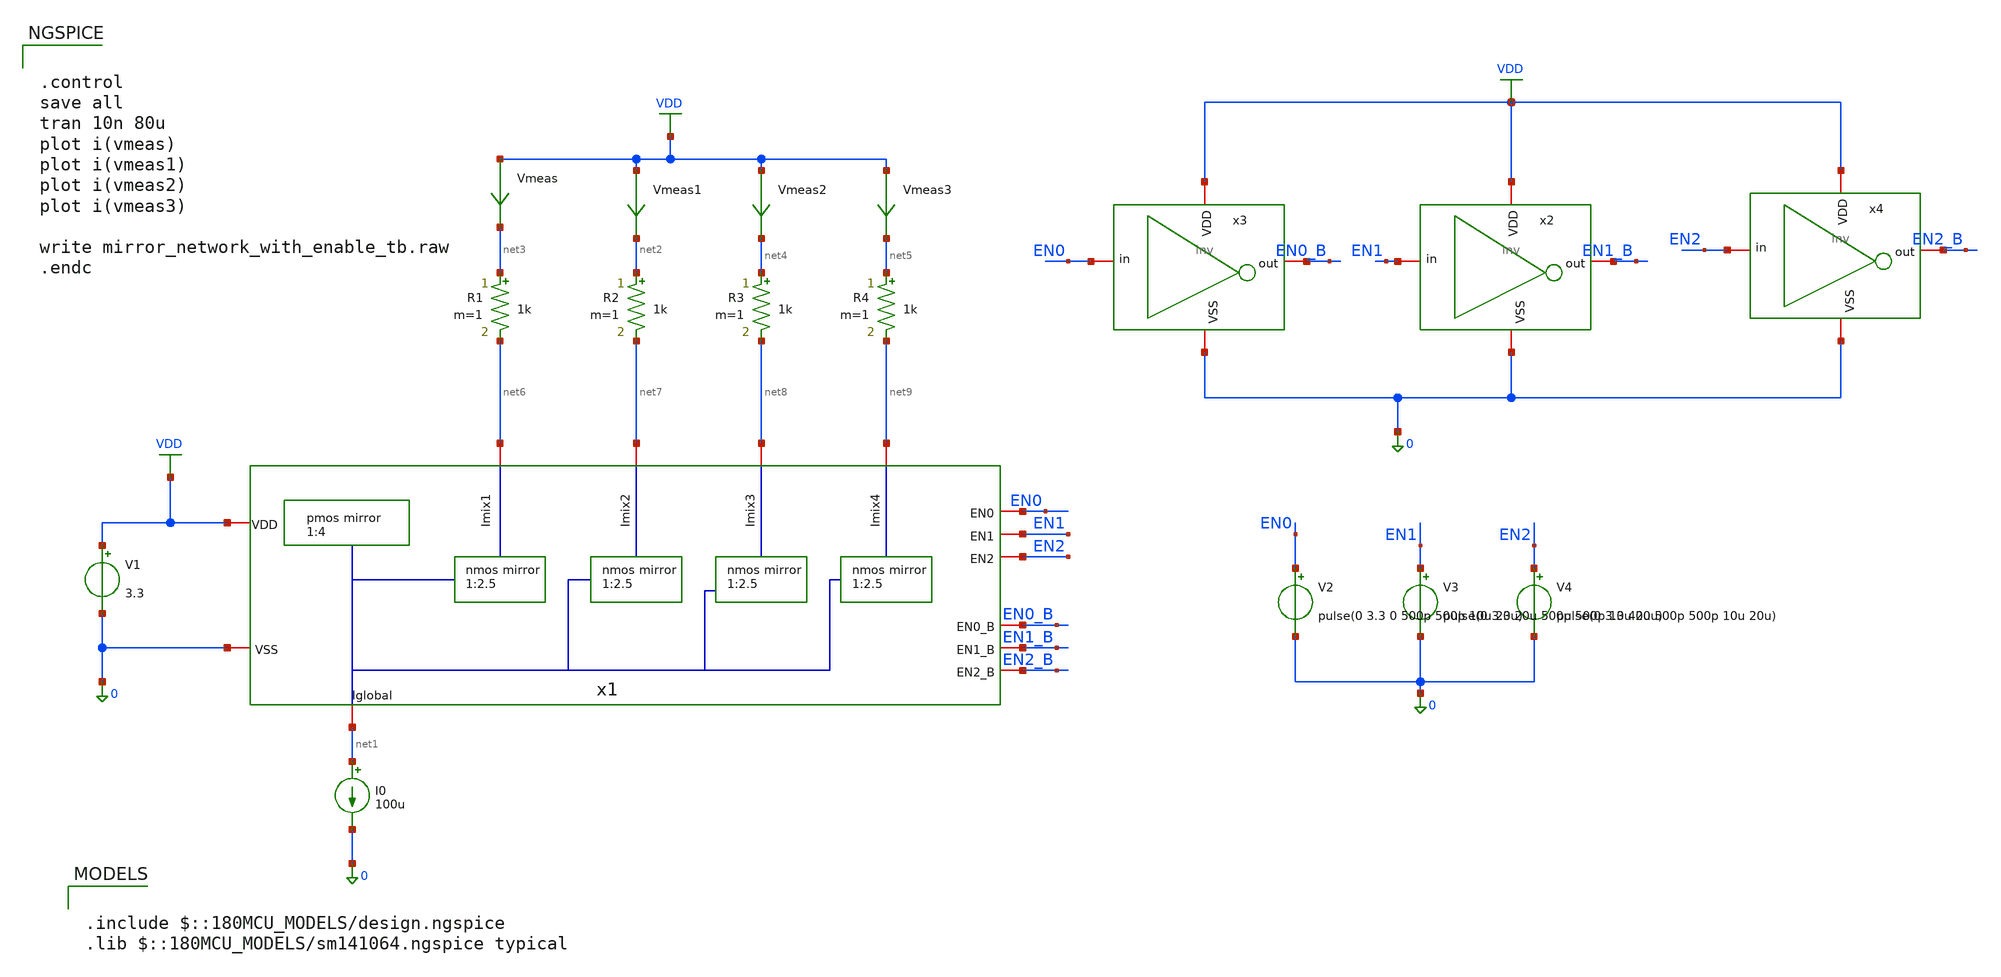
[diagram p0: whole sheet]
** sch_path: designs/mirrors/testbench/mirror_network_with_enable_tb.sch
**.subckt mirror_network_with_enable_tb
V1 VDD 0 3.3
I0 net1 0 100u
R1 net3 net6 1k m=1
R2 net2 net7 1k m=1
R3 net4 net8 1k m=1
R4 net5 net9 1k m=1
Vmeas VDD net3 0
.save i(vmeas)
Vmeas1 VDD net2 0
.save i(vmeas1)
Vmeas2 VDD net4 0
.save i(vmeas2)
Vmeas3 VDD net5 0
.save i(vmeas3)
x2 VDD EN1_B EN1 0 inv
x3 VDD EN0_B EN0 0 inv
x4 VDD EN2_B EN2 0 inv
V2 EN0 0 pulse(0 3.3 0 500p 500p 10u 20u)
V3 EN1 0 pulse(0 3.3 20u 500p 500p 10u 20u)
V4 EN2 0 pulse(0 3.3 40u 500p 500p 10u 20u)
x1 EN2 EN1 EN0 EN0_B EN1_B EN2_B VDD net1 net9 net6 0 net8 net7 mirror_network_with_enable
**** begin user architecture code

.include $::180MCU_MODELS/design.ngspice
.lib $::180MCU_MODELS/sm141064.ngspice typical



.control
save all
tran 10n 80u
plot i(vmeas)
plot i(vmeas1)
plot i(vmeas2)
plot i(vmeas3)

write mirror_network_with_enable_tb.raw
.endc


**** end user architecture code
**.ends
.GLOBAL VDD
.end
